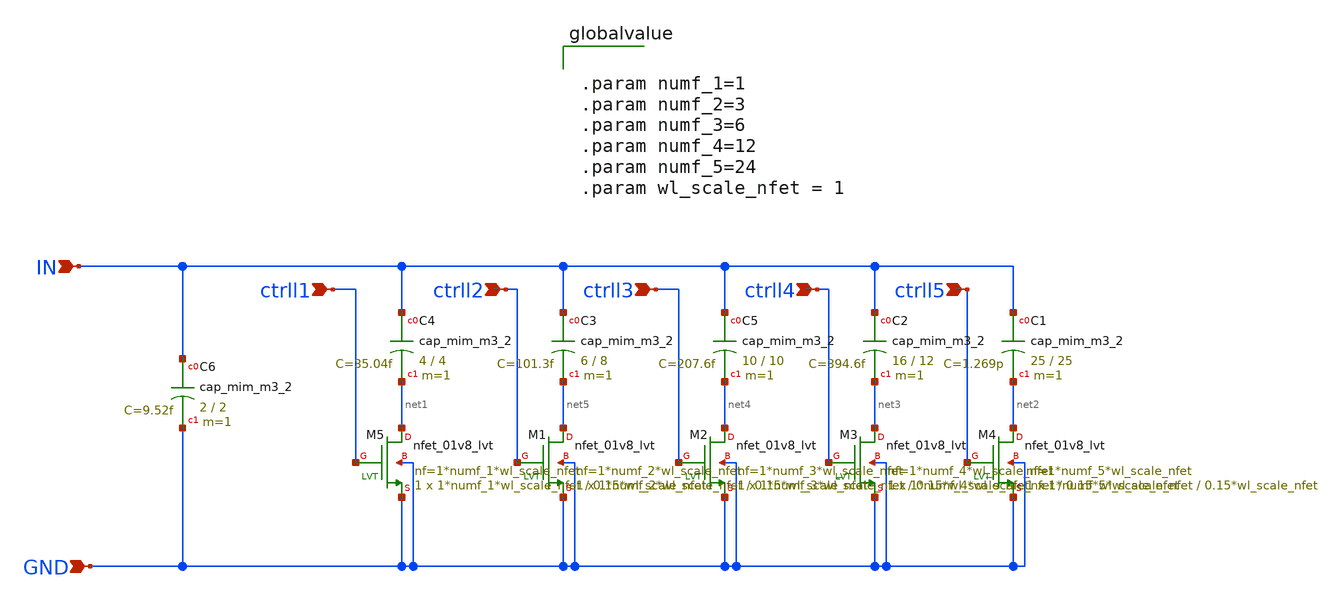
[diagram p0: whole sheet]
** sch_path: design/vco/100M~5G/cap_bank.sch
**.subckt cap_bank IN GND ctrll1 ctrll2 ctrll3 ctrll4 ctrll5
*.ipin IN
*.ipin GND
*.ipin ctrll1
*.ipin ctrll2
*.ipin ctrll3
*.ipin ctrll4
*.ipin ctrll5
XM5 net1 ctrll1 GND GND sky130_fd_pr__nfet_01v8_lvt L=0.15*wl_scale_nfet W=1*numf_1*wl_scale_nfet nf=1*numf_1*wl_scale_nfet
+ ad='int((nf+1)/2) * W/nf * 0.29' as='int((nf+2)/2) * W/nf * 0.29' pd='2*int((nf+1)/2) * (W/nf + 0.29)'
+ ps='2*int((nf+2)/2) * (W/nf + 0.29)' nrd='0.29 / W' nrs='0.29 / W' sa=0 sb=0 sd=0 mult=1 m=1
XM1 net5 ctrll2 GND GND sky130_fd_pr__nfet_01v8_lvt L=0.15*wl_scale_nfet W=1*numf_2*wl_scale_nfet nf=1*numf_2*wl_scale_nfet
+ ad='int((nf+1)/2) * W/nf * 0.29' as='int((nf+2)/2) * W/nf * 0.29' pd='2*int((nf+1)/2) * (W/nf + 0.29)'
+ ps='2*int((nf+2)/2) * (W/nf + 0.29)' nrd='0.29 / W' nrs='0.29 / W' sa=0 sb=0 sd=0 mult=1 m=1
XC4 IN net1 sky130_fd_pr__cap_mim_m3_2 W=4 L=4 MF=1 m=1
XM2 net4 ctrll3 GND GND sky130_fd_pr__nfet_01v8_lvt L=0.15*wl_scale_nfet W=1*numf_3*wl_scale_nfet nf=1*numf_3*wl_scale_nfet
+ ad='int((nf+1)/2) * W/nf * 0.29' as='int((nf+2)/2) * W/nf * 0.29' pd='2*int((nf+1)/2) * (W/nf + 0.29)'
+ ps='2*int((nf+2)/2) * (W/nf + 0.29)' nrd='0.29 / W' nrs='0.29 / W' sa=0 sb=0 sd=0 mult=1 m=1
XM3 net3 ctrll4 GND GND sky130_fd_pr__nfet_01v8_lvt L=0.15*wl_scale_nfet W=1*numf_4*wl_scale_nfet nf=1*numf_4*wl_scale_nfet
+ ad='int((nf+1)/2) * W/nf * 0.29' as='int((nf+2)/2) * W/nf * 0.29' pd='2*int((nf+1)/2) * (W/nf + 0.29)'
+ ps='2*int((nf+2)/2) * (W/nf + 0.29)' nrd='0.29 / W' nrs='0.29 / W' sa=0 sb=0 sd=0 mult=1 m=1
XC2 IN net3 sky130_fd_pr__cap_mim_m3_2 W=16 L=12 MF=1 m=1
XC5 IN net4 sky130_fd_pr__cap_mim_m3_2 W=10 L=10 MF=1 m=1
XC3 IN net5 sky130_fd_pr__cap_mim_m3_2 W=6 L=8 MF=1 m=1
XC1 IN net2 sky130_fd_pr__cap_mim_m3_2 W=25 L=25 MF=1 m=1
XC6 IN GND sky130_fd_pr__cap_mim_m3_2 W=2 L=2 MF=1 m=1
XM4 net2 ctrll5 GND GND sky130_fd_pr__nfet_01v8_lvt L=0.15*wl_scale_nfet W=1*numf_5*wl_scale_nfet nf=1*numf_5*wl_scale_nfet
+ ad='int((nf+1)/2) * W/nf * 0.29' as='int((nf+2)/2) * W/nf * 0.29' pd='2*int((nf+1)/2) * (W/nf + 0.29)'
+ ps='2*int((nf+2)/2) * (W/nf + 0.29)' nrd='0.29 / W' nrs='0.29 / W' sa=0 sb=0 sd=0 mult=1 m=1
**** begin user architecture code


.param numf_1=1
.param numf_2=3
.param numf_3=6
.param numf_4=12
.param numf_5=24
.param wl_scale_nfet = 1


**** end user architecture code
**.ends
.end
